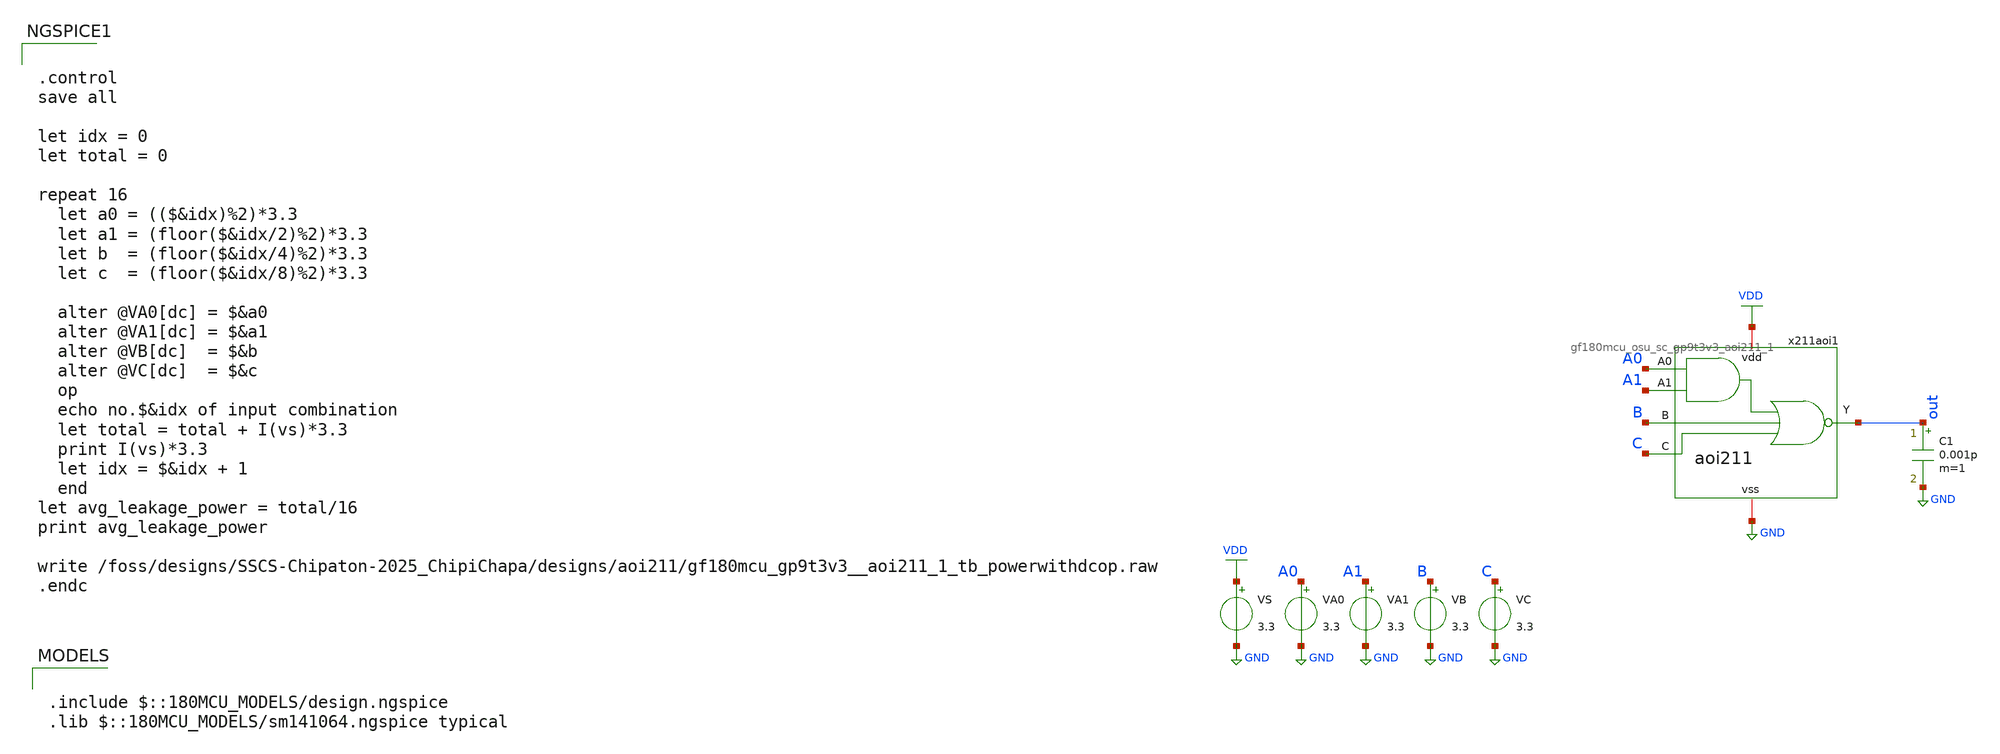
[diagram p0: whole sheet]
** sch_path: designs/aoi211/gf180mcu_osu_gp9t3v3_aoi211_1_tb_powerwithdcop.sch
**.subckt gf180mcu_osu_gp9t3v3_aoi211_1_tb_powerwithdcop
VA0 A0 GND 3.3
VA1 A1 GND 3.3
VB B GND 3.3
VC C GND 3.3
VS VDD GND 3.3
x211aoi1 VDD A1 A0 B C out GND gf180mcu_osu_sc_gp9t3v3_aoi211_1
C1 out GND 0.001p m=1
**** begin user architecture code


.control
save all

let idx = 0
let total = 0

repeat 16
  let a0 = (($&idx)%2)*3.3
  let a1 = (floor($&idx/2)%2)*3.3
  let b  = (floor($&idx/4)%2)*3.3
  let c  = (floor($&idx/8)%2)*3.3

  alter @VA0[dc] = $&a0
  alter @VA1[dc] = $&a1
  alter @VB[dc]  = $&b
  alter @VC[dc]  = $&c
  op
  echo no.$&idx of input combination
  let total = total + I(vs)*3.3
  print I(vs)*3.3
  let idx = $&idx + 1
  end
let avg_leakage_power = total/16
print avg_leakage_power

write
+ /foss/designs/SSCS-Chipaton-2025_ChipiChapa/designs/aoi211/gf180mcu_gp9t3v3__aoi211_1_tb_powerwithdcop.raw
.endc



.include $::180MCU_MODELS/design.ngspice
.lib $::180MCU_MODELS/sm141064.ngspice typical

**** end user architecture code
**.ends
.GLOBAL GND
.GLOBAL VDD
.end
